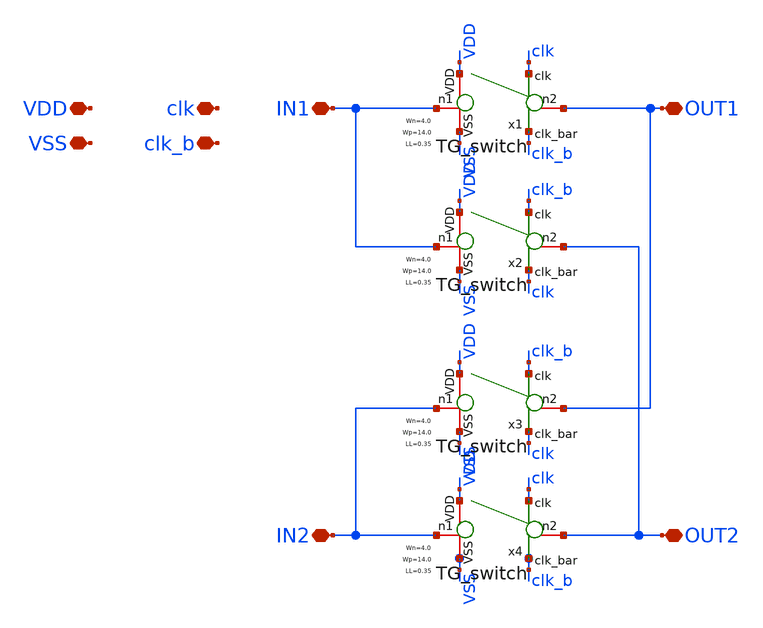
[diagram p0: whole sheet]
** sch_path: xschem/lib/Analog/chopper.sch
**.subckt chopper IN1 IN2 OUT1 OUT2 clk clk_b VDD VSS
*.iopin IN1
*.iopin IN2
*.iopin OUT1
*.iopin OUT2
*.iopin clk
*.iopin clk_b
*.iopin VDD
*.iopin VSS
x1 clk_b clk VDD VSS IN1 OUT1 TG_switch Wn=4.0 Wp=14.0 LL=0.35
x2 clk clk_b VDD VSS IN1 OUT2 TG_switch Wn=4.0 Wp=14.0 LL=0.35
x3 clk clk_b VDD VSS IN2 OUT1 TG_switch Wn=4.0 Wp=14.0 LL=0.35
x4 clk_b clk VDD VSS IN2 OUT2 TG_switch Wn=4.0 Wp=14.0 LL=0.35
**.ends

* expanding   symbol:  Analog/TG_switch.sym # of pins=6
** sym_path: xschem/lib/Analog/TG_switch.sym
** sch_path: xschem/lib/Analog/TG_switch.sch
.subckt TG_switch clk_bar clk VDD VSS n1 n2  Wn=3.0 Wp=10.0 LL=0.35
*.iopin n2
*.iopin n1
*.iopin VDD
*.iopin VSS
*.ipin clk_bar
*.ipin clk
XM3 n1 clk n2 VSS sky130_fd_pr__nfet_01v8_lvt L=LL W=Wn nf=1 ad='int((1 + 1)/2) * Wn / 1 * 0.29' as='int((1 + 2)/2) * Wn / 1 * 0.29'
+ pd='2*int((1 + 1)/2) * (Wn / 1 + 0.29)' ps='2*int((1 + 2)/2) * (Wn / 1 + 0.29)' nrd='0.29 / Wn ' nrs='0.29 / Wn '
+ sa=0 sb=0 sd=0 mult=1 m=1
XM4 n1 clk_bar n2 VDD sky130_fd_pr__pfet_01v8_lvt L=LL W=Wp nf=1 ad='int((1 + 1)/2) * Wp / 1 * 0.29'
+ as='int((1 + 2)/2) * Wp / 1 * 0.29' pd='2*int((1 + 1)/2) * (Wp / 1 + 0.29)' ps='2*int((1 + 2)/2) * (Wp / 1 + 0.29)'
+ nrd='0.29 / Wp ' nrs='0.29 / Wp ' sa=0 sb=0 sd=0 mult=1 m=1
.ends

.end
